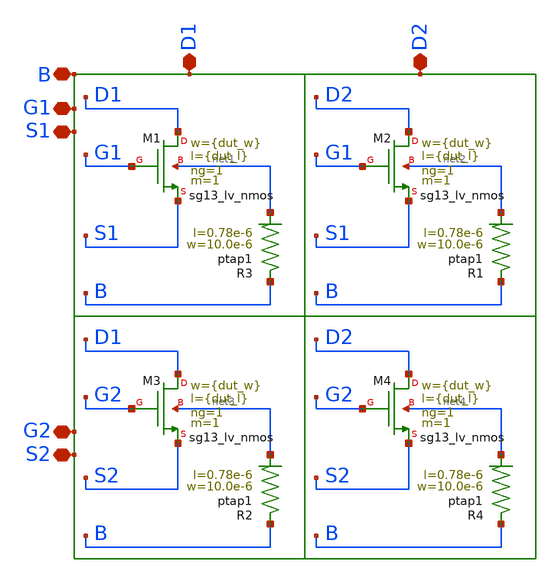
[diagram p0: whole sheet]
** sch_path: design_data/xschem/DUT.sch
**.subckt DUT S1 G1 D1 B S2 G2 D2
*.iopin S1
*.iopin G1
*.iopin D1
*.iopin B
*.iopin S2
*.iopin G2
*.iopin D2
XM1 D1 G1 S1 net1 sg13_lv_nmos w={dut_w} l={dut_l} ng=1 m=1 mm_ok=1
XR3 B net1 ptap1 R=33.38 w=10.0e-6 l=0.78e-6
XM2 D2 G1 S1 net2 sg13_lv_nmos w={dut_w} l={dut_l} ng=1 m=1 mm_ok=1
XR1 B net2 ptap1 R=33.38 w=10.0e-6 l=0.78e-6
XM3 D1 G2 S2 net3 sg13_lv_nmos w={dut_w} l={dut_l} ng=1 m=1 mm_ok=1
XR2 B net3 ptap1 R=33.38 w=10.0e-6 l=0.78e-6
XM4 D2 G2 S2 net4 sg13_lv_nmos w={dut_w} l={dut_l} ng=1 m=1 mm_ok=1
XR4 B net4 ptap1 R=33.38 w=10.0e-6 l=0.78e-6
**.ends
.end
